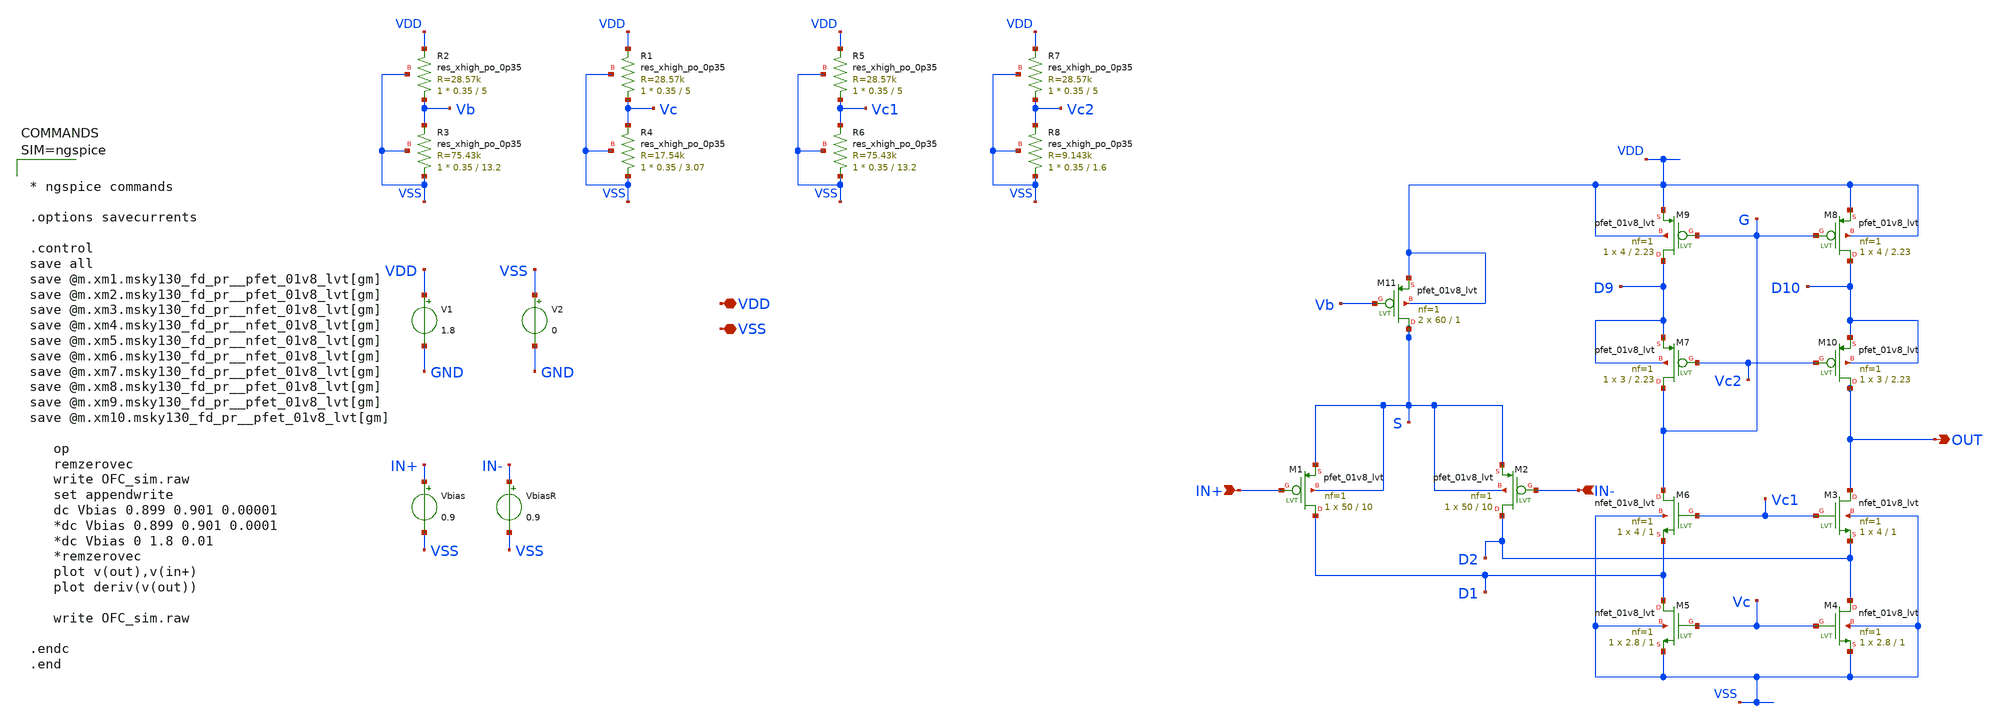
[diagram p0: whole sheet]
** sch_path: tt_um_NE567Mixer28/xschem/OFC_sim.sch
**.subckt OFC_sim VDD VSS IN+ IN- OUT
*.iopin VDD
*.iopin VSS
*.ipin IN+
*.ipin IN-
*.opin OUT
V1 VDD GND 1.8
Vbias IN+ VSS 0.9
VbiasR IN- VSS 0.9
XM11 S Vb VDD VDD sky130_fd_pr__pfet_01v8_lvt L=1 W=60 nf=1 ad='int((nf+1)/2) * W/nf * 0.29' as='int((nf+2)/2) * W/nf * 0.29'
+ pd='2*int((nf+1)/2) * (W/nf + 0.29)' ps='2*int((nf+2)/2) * (W/nf + 0.29)' nrd='0.29 / W' nrs='0.29 / W'
+ sa=0 sb=0 sd=0 mult=2 m=2
XM1 D1 IN+ S S sky130_fd_pr__pfet_01v8_lvt L=10 W=50 nf=1 ad='int((nf+1)/2) * W/nf * 0.29' as='int((nf+2)/2) * W/nf * 0.29'
+ pd='2*int((nf+1)/2) * (W/nf + 0.29)' ps='2*int((nf+2)/2) * (W/nf + 0.29)' nrd='0.29 / W' nrs='0.29 / W'
+ sa=0 sb=0 sd=0 mult=1 m=1
XM2 D2 IN- S S sky130_fd_pr__pfet_01v8_lvt L=10 W=50 nf=1 ad='int((nf+1)/2) * W/nf * 0.29' as='int((nf+2)/2) * W/nf * 0.29'
+ pd='2*int((nf+1)/2) * (W/nf + 0.29)' ps='2*int((nf+2)/2) * (W/nf + 0.29)' nrd='0.29 / W' nrs='0.29 / W'
+ sa=0 sb=0 sd=0 mult=1 m=1
XM3 OUT Vc1 D2 VSS sky130_fd_pr__nfet_01v8_lvt L=1 W=4 nf=1 ad='int((nf+1)/2) * W/nf * 0.29' as='int((nf+2)/2) * W/nf * 0.29'
+ pd='2*int((nf+1)/2) * (W/nf + 0.29)' ps='2*int((nf+2)/2) * (W/nf + 0.29)' nrd='0.29 / W' nrs='0.29 / W'
+ sa=0 sb=0 sd=0 mult=1 m=1
XM4 D2 Vc VSS VSS sky130_fd_pr__nfet_01v8_lvt L=1 W=2.8 nf=1 ad='int((nf+1)/2) * W/nf * 0.29' as='int((nf+2)/2) * W/nf * 0.29'
+ pd='2*int((nf+1)/2) * (W/nf + 0.29)' ps='2*int((nf+2)/2) * (W/nf + 0.29)' nrd='0.29 / W' nrs='0.29 / W'
+ sa=0 sb=0 sd=0 mult=1 m=1
XM5 D1 Vc VSS VSS sky130_fd_pr__nfet_01v8_lvt L=1 W=2.8 nf=1 ad='int((nf+1)/2) * W/nf * 0.29' as='int((nf+2)/2) * W/nf * 0.29'
+ pd='2*int((nf+1)/2) * (W/nf + 0.29)' ps='2*int((nf+2)/2) * (W/nf + 0.29)' nrd='0.29 / W' nrs='0.29 / W'
+ sa=0 sb=0 sd=0 mult=1 m=1
XM6 G Vc1 D1 VSS sky130_fd_pr__nfet_01v8_lvt L=1 W=4 nf=1 ad='int((nf+1)/2) * W/nf * 0.29' as='int((nf+2)/2) * W/nf * 0.29'
+ pd='2*int((nf+1)/2) * (W/nf + 0.29)' ps='2*int((nf+2)/2) * (W/nf + 0.29)' nrd='0.29 / W' nrs='0.29 / W'
+ sa=0 sb=0 sd=0 mult=1 m=1
XM7 G Vc2 D9 D9 sky130_fd_pr__pfet_01v8_lvt L=2.23 W=3 nf=1 ad='int((nf+1)/2) * W/nf * 0.29' as='int((nf+2)/2) * W/nf * 0.29'
+ pd='2*int((nf+1)/2) * (W/nf + 0.29)' ps='2*int((nf+2)/2) * (W/nf + 0.29)' nrd='0.29 / W' nrs='0.29 / W'
+ sa=0 sb=0 sd=0 mult=1 m=1
XM9 D9 G VDD VDD sky130_fd_pr__pfet_01v8_lvt L=2.23 W=4 nf=1 ad='int((nf+1)/2) * W/nf * 0.29' as='int((nf+2)/2) * W/nf * 0.29'
+ pd='2*int((nf+1)/2) * (W/nf + 0.29)' ps='2*int((nf+2)/2) * (W/nf + 0.29)' nrd='0.29 / W' nrs='0.29 / W'
+ sa=0 sb=0 sd=0 mult=1 m=1
XM8 D10 G VDD VDD sky130_fd_pr__pfet_01v8_lvt L=2.23 W=4 nf=1 ad='int((nf+1)/2) * W/nf * 0.29' as='int((nf+2)/2) * W/nf * 0.29'
+ pd='2*int((nf+1)/2) * (W/nf + 0.29)' ps='2*int((nf+2)/2) * (W/nf + 0.29)' nrd='0.29 / W' nrs='0.29 / W'
+ sa=0 sb=0 sd=0 mult=1 m=1
XM10 OUT Vc2 D10 D10 sky130_fd_pr__pfet_01v8_lvt L=2.23 W=3 nf=1 ad='int((nf+1)/2) * W/nf * 0.29' as='int((nf+2)/2) * W/nf * 0.29'
+ pd='2*int((nf+1)/2) * (W/nf + 0.29)' ps='2*int((nf+2)/2) * (W/nf + 0.29)' nrd='0.29 / W' nrs='0.29 / W'
+ sa=0 sb=0 sd=0 mult=1 m=1
XR2 Vb VDD VSS sky130_fd_pr__res_xhigh_po_0p35 L=5 mult=1 m=1
XR3 VSS Vb VSS sky130_fd_pr__res_xhigh_po_0p35 L=13.2 mult=1 m=1
XR1 Vc VDD VSS sky130_fd_pr__res_xhigh_po_0p35 L=5 mult=1 m=1
XR4 VSS Vc VSS sky130_fd_pr__res_xhigh_po_0p35 L=3.07 mult=1 m=1
XR5 Vc1 VDD VSS sky130_fd_pr__res_xhigh_po_0p35 L=5 mult=1 m=1
XR6 VSS Vc1 VSS sky130_fd_pr__res_xhigh_po_0p35 L=13.2 mult=1 m=1
XR7 Vc2 VDD VSS sky130_fd_pr__res_xhigh_po_0p35 L=5 mult=1 m=1
XR8 VSS Vc2 VSS sky130_fd_pr__res_xhigh_po_0p35 L=1.6 mult=1 m=1
V2 VSS GND 0
**** begin user architecture code



* ngspice commands

.options savecurrents

.control
save all
save @m.xm1.msky130_fd_pr__pfet_01v8_lvt[gm]
save @m.xm2.msky130_fd_pr__pfet_01v8_lvt[gm]
save @m.xm3.msky130_fd_pr__nfet_01v8_lvt[gm]
save @m.xm4.msky130_fd_pr__nfet_01v8_lvt[gm]
save @m.xm5.msky130_fd_pr__nfet_01v8_lvt[gm]
save @m.xm6.msky130_fd_pr__nfet_01v8_lvt[gm]
save @m.xm7.msky130_fd_pr__pfet_01v8_lvt[gm]
save @m.xm8.msky130_fd_pr__pfet_01v8_lvt[gm]
save @m.xm9.msky130_fd_pr__pfet_01v8_lvt[gm]
save @m.xm10.msky130_fd_pr__pfet_01v8_lvt[gm]

   op
   remzerovec
   write OFC_sim.raw
   set appendwrite
   dc Vbias 0.899 0.901 0.00001
   *dc Vbias 0.899 0.901 0.0001
   *dc Vbias 0 1.8 0.01
   *remzerovec
   plot v(out),v(in+)
   plot deriv(v(out))

   write OFC_sim.raw

.endc
.end



.lib $::SKYWATER_MODELS/sky130.lib.spice tt
**** end user architecture code
**.ends
.end
